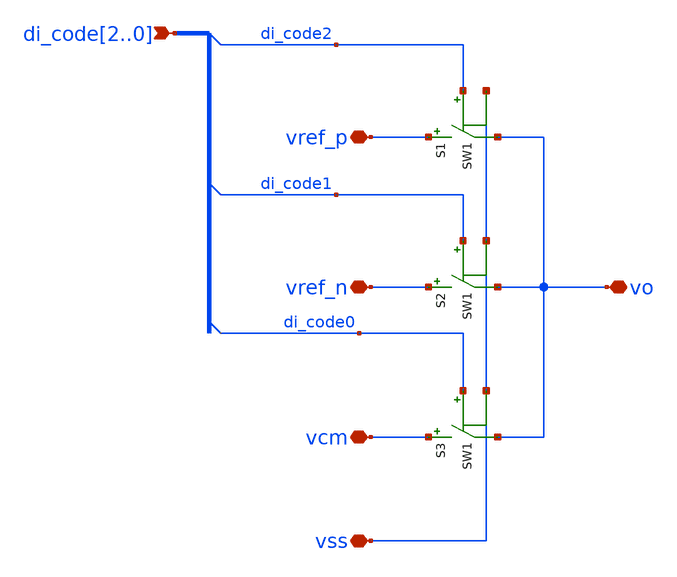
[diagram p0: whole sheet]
** sch_path: xschem/sw_dac.sch
**.subckt sw_dac di_code2,di_code1,di_code0 vref_p vref_n vo vss vcm
*.ipin di_code2,di_code1,di_code0
*.iopin vref_p
*.iopin vref_n
*.iopin vo
*.iopin vss
*.iopin vcm
S1 vref_p vo di_code2 vss SW1
S2 vref_n vo di_code1 vss SW1
S3 vcm vo di_code0 vss SW1
**.ends
**** begin user architecture code
.MODEL SW1 SW( VT=0.75 VH=0.01 RON=ron ROFF=roff )
**** end user architecture code
.end
